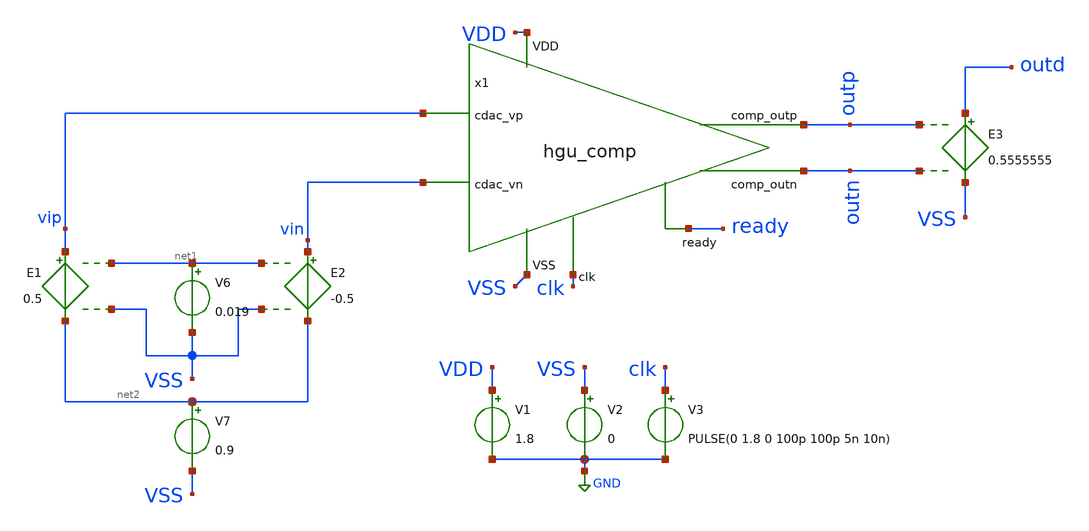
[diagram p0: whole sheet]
** sch_path: hgu/tb/tb_hgu_comp_MC_sim.sch
**.subckt tb_hgu_comp_MC_sim
x1 ready vin outp outn vip clk VDD VSS hgu_comp
V1 VDD GND 1.8
V2 VSS GND 0
V3 clk GND PULSE(0 1.8 0 100p 100p 5n 10n)
E1 vip net2 net1 VSS 0.5
E2 vin net2 net1 VSS -0.5
V6 net1 VSS 0.019
V7 net2 VSS 0.9
E3 outd VSS outp outn 0.5555555
**** begin user architecture code



.include /foss/designs/hgu_goss/hgu/spice/hgu_comp_flat_RC.spice
.lib /foss/pdks/sky130A/libs.tech/ngspice/sky130.lib.spice tt_mm
.include /foss/pdks/sky130A/libs.ref/sky130_fd_sc_hd/spice/sky130_fd_sc_hd.spice
.tran 0.1ns 10ns
.temp 25
.control
    repeat 100

    tran 0.1ns 10ns
    print avg V(outd)
    write test_mc_model.txt
    set appendwrite
    reset

    end
	meas tran v1 AVG tran1.v(outd) FROM=2n TO=10n
	meas tran v2 AVG tran2.v(outd) FROM=2n TO=10n
	meas tran v3 AVG tran3.v(outd) FROM=2n TO=10n
	meas tran v4 AVG tran4.v(outd) FROM=2n TO=10n
	meas tran v5 AVG tran5.v(outd) FROM=2n TO=10n
	meas tran v6 AVG tran6.v(outd) FROM=2n TO=10n
	meas tran v7 AVG tran7.v(outd) FROM=2n TO=10n
	meas tran v8 AVG tran8.v(outd) FROM=2n TO=10n
	meas tran v9 AVG tran9.v(outd) FROM=2n TO=10n
	meas tran v10 AVG tran10.v(outd) FROM=2n TO=10n
	let avg_v1 = (v1+v2+v3+v4+v5+v6+v7+v8+v9+v10)/10

	meas tran v11 AVG tran11.v(outd) FROM=2n TO=10n
	meas tran v12 AVG tran12.v(outd) FROM=2n TO=10n
	meas tran v13 AVG tran13.v(outd) FROM=2n TO=10n
	meas tran v14 AVG tran14.v(outd) FROM=2n TO=10n
	meas tran v15 AVG tran15.v(outd) FROM=2n TO=10n
	meas tran v16 AVG tran16.v(outd) FROM=2n TO=10n
	meas tran v17 AVG tran17.v(outd) FROM=2n TO=10n
	meas tran v18 AVG tran18.v(outd) FROM=2n TO=10n
	meas tran v19 AVG tran19.v(outd) FROM=2n TO=10n
	meas tran v20 AVG tran20.v(outd) FROM=2n TO=10n
	let avg_v2 = (v11+v12+v13+v14+v15+v16+v17+v18+v19+v20)/10


	meas tran v21 AVG tran21.v(outd) FROM=2n TO=10n
	meas tran v22 AVG tran22.v(outd) FROM=2n TO=10n
	meas tran v23 AVG tran23.v(outd) FROM=2n TO=10n
	meas tran v24 AVG tran24.v(outd) FROM=2n TO=10n
	meas tran v25 AVG tran25.v(outd) FROM=2n TO=10n
	meas tran v26 AVG tran26.v(outd) FROM=2n TO=10n
	meas tran v27 AVG tran27.v(outd) FROM=2n TO=10n
	meas tran v28 AVG tran28.v(outd) FROM=2n TO=10n
	meas tran v29 AVG tran29.v(outd) FROM=2n TO=10n
	meas tran v30 AVG tran30.v(outd) FROM=2n TO=10n
	let avg_v3 = (v21+v22+v23+v24+v25+v26+v27+v28+v29+v30)/10

	meas tran v31 AVG tran31.v(outd) FROM=2n TO=10n
	meas tran v32 AVG tran32.v(outd) FROM=2n TO=10n
	meas tran v33 AVG tran33.v(outd) FROM=2n TO=10n
	meas tran v34 AVG tran34.v(outd) FROM=2n TO=10n
	meas tran v35 AVG tran35.v(outd) FROM=2n TO=10n
	meas tran v36 AVG tran36.v(outd) FROM=2n TO=10n
	meas tran v37 AVG tran37.v(outd) FROM=2n TO=10n
	meas tran v38 AVG tran38.v(outd) FROM=2n TO=10n
	meas tran v39 AVG tran39.v(outd) FROM=2n TO=10n
	meas tran v40 AVG tran40.v(outd) FROM=2n TO=10n
	let avg_v4 = (v31+v32+v33+v34+v35+v36+v37+v38+v39+v40)/10

	meas tran v41 AVG tran41.v(outd) FROM=2n TO=10n
	meas tran v42 AVG tran42.v(outd) FROM=2n TO=10n
	meas tran v43 AVG tran43.v(outd) FROM=2n TO=10n
	meas tran v44 AVG tran44.v(outd) FROM=2n TO=10n
	meas tran v45 AVG tran45.v(outd) FROM=2n TO=10n
	meas tran v46 AVG tran46.v(outd) FROM=2n TO=10n
	meas tran v47 AVG tran47.v(outd) FROM=2n TO=10n
	meas tran v48 AVG tran48.v(outd) FROM=2n TO=10n
	meas tran v49 AVG tran49.v(outd) FROM=2n TO=10n
	meas tran v50 AVG tran50.v(outd) FROM=2n TO=10n
	let avg_v5 = (v41+v42+v43+v44+v45+v46+v47+v48+v49+v50)/10

	meas tran v51 AVG tran51.v(outd) FROM=2n TO=10n
	meas tran v52 AVG tran52.v(outd) FROM=2n TO=10n
	meas tran v53 AVG tran53.v(outd) FROM=2n TO=10n
	meas tran v54 AVG tran54.v(outd) FROM=2n TO=10n
	meas tran v55 AVG tran55.v(outd) FROM=2n TO=10n
	meas tran v56 AVG tran56.v(outd) FROM=2n TO=10n
	meas tran v57 AVG tran57.v(outd) FROM=2n TO=10n
	meas tran v58 AVG tran58.v(outd) FROM=2n TO=10n
	meas tran v59 AVG tran59.v(outd) FROM=2n TO=10n
	meas tran v60 AVG tran60.v(outd) FROM=2n TO=10n
	let avg_v6 = (v51+v52+v53+v54+v55+v56+v57+v58+v59+v60)/10

	meas tran v61 AVG tran61.v(outd) FROM=2n TO=10n
	meas tran v62 AVG tran62.v(outd) FROM=2n TO=10n
	meas tran v63 AVG tran63.v(outd) FROM=2n TO=10n
	meas tran v64 AVG tran64.v(outd) FROM=2n TO=10n
	meas tran v65 AVG tran65.v(outd) FROM=2n TO=10n
	meas tran v66 AVG tran66.v(outd) FROM=2n TO=10n
	meas tran v67 AVG tran67.v(outd) FROM=2n TO=10n
	meas tran v68 AVG tran68.v(outd) FROM=2n TO=10n
	meas tran v69 AVG tran69.v(outd) FROM=2n TO=10n
	meas tran v70 AVG tran70.v(outd) FROM=2n TO=10n
	let avg_v7 = (v61+v62+v63+v64+v65+v66+v67+v68+v69+v70)/10

	meas tran v71 AVG tran71.v(outd) FROM=2n TO=10n
	meas tran v72 AVG tran72.v(outd) FROM=2n TO=10n
	meas tran v73 AVG tran73.v(outd) FROM=2n TO=10n
	meas tran v74 AVG tran74.v(outd) FROM=2n TO=10n
	meas tran v75 AVG tran75.v(outd) FROM=2n TO=10n
	meas tran v76 AVG tran76.v(outd) FROM=2n TO=10n
	meas tran v77 AVG tran77.v(outd) FROM=2n TO=10n
	meas tran v78 AVG tran78.v(outd) FROM=2n TO=10n
	meas tran v79 AVG tran79.v(outd) FROM=2n TO=10n
	meas tran v80 AVG tran80.v(outd) FROM=2n TO=10n
	let avg_v8 = (v71+v72+v73+v74+v75+v76+v77+v78+v79+v80)/10

	meas tran v81 AVG tran81.v(outd) FROM=2n TO=10n
	meas tran v82 AVG tran82.v(outd) FROM=2n TO=10n
	meas tran v83 AVG tran83.v(outd) FROM=2n TO=10n
	meas tran v84 AVG tran84.v(outd) FROM=2n TO=10n
	meas tran v85 AVG tran85.v(outd) FROM=2n TO=10n
	meas tran v86 AVG tran86.v(outd) FROM=2n TO=10n
	meas tran v87 AVG tran87.v(outd) FROM=2n TO=10n
	meas tran v88 AVG tran88.v(outd) FROM=2n TO=10n
	meas tran v89 AVG tran89.v(outd) FROM=2n TO=10n
	meas tran v90 AVG tran90.v(outd) FROM=2n TO=10n
	let avg_v9 = (v81+v82+v83+v84+v85+v86+v87+v88+v89+v90)/10

	meas tran v91 AVG tran91.v(outd) FROM=2n TO=10n
	meas tran v92 AVG tran92.v(outd) FROM=2n TO=10n
	meas tran v93 AVG tran93.v(outd) FROM=2n TO=10n
	meas tran v94 AVG tran94.v(outd) FROM=2n TO=10n
	meas tran v95 AVG tran95.v(outd) FROM=2n TO=10n
	meas tran v96 AVG tran96.v(outd) FROM=2n TO=10n
	meas tran v97 AVG tran97.v(outd) FROM=2n TO=10n
	meas tran v98 AVG tran98.v(outd) FROM=2n TO=10n
	meas tran v99 AVG tran99.v(outd) FROM=2n TO=10n
	meas tran v100 AVG tran100.v(outd) FROM=2n TO=10n
	let avg_v10 = (v91+v92+v93+v94+v95+v96+v97+v98+v99+v100)/10

    let final_avg = (avg_v1+avg_v2+avg_v3+avg_v4+avg_v5+avg_v6+avg_v7+avg_v8+avg_v9+avg_v10)/10
    *plot all.v(outd)
    print final_avg
.endc
.save all


**** end user architecture code
**.ends

* expanding   symbol:  ../xschem/hgu_comp.sym # of pins=8
** sym_path: hgu/xschem/hgu_comp.sym
** sch_path: hgu/xschem/hgu_comp.sch
.subckt hgu_comp ready cdac_vn comp_outp comp_outn cdac_vp clk VDD VSS
*.ipin cdac_vn
*.ipin cdac_vp
*.ipin VSS
*.ipin VDD
*.ipin clk
*.opin ready
*.opin comp_outp
*.opin comp_outn
XM1 net1 clk VSS VSS sky130_fd_pr__nfet_01v8 L=0.15 W=4 nf=4 ad='int((nf+1)/2) * W/nf * 0.29' as='int((nf+2)/2) * W/nf * 0.29'
+ pd='2*int((nf+1)/2) * (W/nf + 0.29)' ps='2*int((nf+2)/2) * (W/nf + 0.29)' nrd='0.29 / W' nrs='0.29 / W'
+ sa=0 sb=0 sd=0 mult=1 m=1
XM4 Y X Q VSS sky130_fd_pr__nfet_01v8 L=0.15 W=1 nf=1 ad='int((nf+1)/2) * W/nf * 0.29' as='int((nf+2)/2) * W/nf * 0.29'
+ pd='2*int((nf+1)/2) * (W/nf + 0.29)' ps='2*int((nf+2)/2) * (W/nf + 0.29)' nrd='0.29 / W' nrs='0.29 / W'
+ sa=0 sb=0 sd=0 mult=1 m=1
XM5 X Y P VSS sky130_fd_pr__nfet_01v8 L=0.15 W=1 nf=1 ad='int((nf+1)/2) * W/nf * 0.29' as='int((nf+2)/2) * W/nf * 0.29'
+ pd='2*int((nf+1)/2) * (W/nf + 0.29)' ps='2*int((nf+2)/2) * (W/nf + 0.29)' nrd='0.29 / W' nrs='0.29 / W'
+ sa=0 sb=0 sd=0 mult=1 m=1
XM6 X Y VDD VDD sky130_fd_pr__pfet_01v8 L=0.15 W=1 nf=1 ad='int((nf+1)/2) * W/nf * 0.29' as='int((nf+2)/2) * W/nf * 0.29'
+ pd='2*int((nf+1)/2) * (W/nf + 0.29)' ps='2*int((nf+2)/2) * (W/nf + 0.29)' nrd='0.29 / W' nrs='0.29 / W'
+ sa=0 sb=0 sd=0 mult=1 m=1
XM7 Y X VDD VDD sky130_fd_pr__pfet_01v8 L=0.15 W=1 nf=1 ad='int((nf+1)/2) * W/nf * 0.29' as='int((nf+2)/2) * W/nf * 0.29'
+ pd='2*int((nf+1)/2) * (W/nf + 0.29)' ps='2*int((nf+2)/2) * (W/nf + 0.29)' nrd='0.29 / W' nrs='0.29 / W'
+ sa=0 sb=0 sd=0 mult=1 m=1
XM8 X clk VDD VDD sky130_fd_pr__pfet_01v8 L=0.15 W=1 nf=1 ad='int((nf+1)/2) * W/nf * 0.29' as='int((nf+2)/2) * W/nf * 0.29'
+ pd='2*int((nf+1)/2) * (W/nf + 0.29)' ps='2*int((nf+2)/2) * (W/nf + 0.29)' nrd='0.29 / W' nrs='0.29 / W'
+ sa=0 sb=0 sd=0 mult=1 m=1
XM9 P clk VDD VDD sky130_fd_pr__pfet_01v8 L=0.15 W=1 nf=1 ad='int((nf+1)/2) * W/nf * 0.29' as='int((nf+2)/2) * W/nf * 0.29'
+ pd='2*int((nf+1)/2) * (W/nf + 0.29)' ps='2*int((nf+2)/2) * (W/nf + 0.29)' nrd='0.29 / W' nrs='0.29 / W'
+ sa=0 sb=0 sd=0 mult=1 m=1
XM10 Y clk VDD VDD sky130_fd_pr__pfet_01v8 L=0.15 W=1 nf=1 ad='int((nf+1)/2) * W/nf * 0.29' as='int((nf+2)/2) * W/nf * 0.29'
+ pd='2*int((nf+1)/2) * (W/nf + 0.29)' ps='2*int((nf+2)/2) * (W/nf + 0.29)' nrd='0.29 / W' nrs='0.29 / W'
+ sa=0 sb=0 sd=0 mult=1 m=1
XM11 Q clk VDD VDD sky130_fd_pr__pfet_01v8 L=0.15 W=1 nf=1 ad='int((nf+1)/2) * W/nf * 0.29' as='int((nf+2)/2) * W/nf * 0.29'
+ pd='2*int((nf+1)/2) * (W/nf + 0.29)' ps='2*int((nf+2)/2) * (W/nf + 0.29)' nrd='0.29 / W' nrs='0.29 / W'
+ sa=0 sb=0 sd=0 mult=1 m=1
XM16 RS_n RS_p VDD VDD sky130_fd_pr__pfet_01v8 L=0.15 W=0.84 nf=1 ad='int((nf+1)/2) * W/nf * 0.29' as='int((nf+2)/2) * W/nf * 0.29'
+ pd='2*int((nf+1)/2) * (W/nf + 0.29)' ps='2*int((nf+2)/2) * (W/nf + 0.29)' nrd='0.29 / W' nrs='0.29 / W'
+ sa=0 sb=0 sd=0 mult=1 m=1
XM17 RS_p RS_n VDD VDD sky130_fd_pr__pfet_01v8 L=0.15 W=0.84 nf=1 ad='int((nf+1)/2) * W/nf * 0.29' as='int((nf+2)/2) * W/nf * 0.29'
+ pd='2*int((nf+1)/2) * (W/nf + 0.29)' ps='2*int((nf+2)/2) * (W/nf + 0.29)' nrd='0.29 / W' nrs='0.29 / W'
+ sa=0 sb=0 sd=0 mult=1 m=1
XM19 RS_p Y_inv VSS VSS sky130_fd_pr__nfet_01v8 L=0.15 W=0.84 nf=1 ad='int((nf+1)/2) * W/nf * 0.29' as='int((nf+2)/2) * W/nf * 0.29'
+ pd='2*int((nf+1)/2) * (W/nf + 0.29)' ps='2*int((nf+2)/2) * (W/nf + 0.29)' nrd='0.29 / W' nrs='0.29 / W'
+ sa=0 sb=0 sd=0 mult=1 m=1
XM23 RS_n X_inv VSS VSS sky130_fd_pr__nfet_01v8 L=0.15 W=0.84 nf=1 ad='int((nf+1)/2) * W/nf * 0.29' as='int((nf+2)/2) * W/nf * 0.29'
+ pd='2*int((nf+1)/2) * (W/nf + 0.29)' ps='2*int((nf+2)/2) * (W/nf + 0.29)' nrd='0.29 / W' nrs='0.29 / W'
+ sa=0 sb=0 sd=0 mult=1 m=1
XM2 P cdac_vp net1 VSS sky130_fd_pr__nfet_01v8_lvt L=0.15 W=8 nf=8 ad='int((nf+1)/2) * W / nf * 0.29'
+ as='int((nf+2)/2) * W / nf * 0.29' pd='2*int((nf+1)/2) * (W / nf + 0.29)' ps='2*int((nf+2)/2) * (W / nf + 0.29)'
+ nrd='0.29 / W ' nrs='0.29 / W ' sa=0 sb=0 sd=0 mult=1 m=1
XM3 Q cdac_vn net1 VSS sky130_fd_pr__nfet_01v8_lvt L=0.15 W=8 nf=8 ad='int((nf+1)/2) * W / nf * 0.29'
+ as='int((nf+2)/2) * W / nf * 0.29' pd='2*int((nf+1)/2) * (W / nf + 0.29)' ps='2*int((nf+2)/2) * (W / nf + 0.29)'
+ nrd='0.29 / W ' nrs='0.29 / W ' sa=0 sb=0 sd=0 mult=1 m=1
XM12 X_inv X VDD VDD sky130_fd_pr__pfet_01v8 L=0.15 W=0.84 nf=1 ad='int((nf+1)/2) * W/nf * 0.29' as='int((nf+2)/2) * W/nf * 0.29'
+ pd='2*int((nf+1)/2) * (W/nf + 0.29)' ps='2*int((nf+2)/2) * (W/nf + 0.29)' nrd='0.29 / W' nrs='0.29 / W'
+ sa=0 sb=0 sd=0 mult=1 m=1
XM13 X_inv X VSS VSS sky130_fd_pr__nfet_01v8 L=0.15 W=0.42 nf=1 ad='int((nf+1)/2) * W/nf * 0.29' as='int((nf+2)/2) * W/nf * 0.29'
+ pd='2*int((nf+1)/2) * (W/nf + 0.29)' ps='2*int((nf+2)/2) * (W/nf + 0.29)' nrd='0.29 / W' nrs='0.29 / W'
+ sa=0 sb=0 sd=0 mult=1 m=1
XM14 X_drive X_inv VDD VDD sky130_fd_pr__pfet_01v8 L=0.15 W=2.52 nf=3 ad='int((nf+1)/2) * W/nf * 0.29'
+ as='int((nf+2)/2) * W/nf * 0.29' pd='2*int((nf+1)/2) * (W/nf + 0.29)' ps='2*int((nf+2)/2) * (W/nf + 0.29)'
+ nrd='0.29 / W' nrs='0.29 / W' sa=0 sb=0 sd=0 mult=1 m=1
XM15 X_drive X_inv VSS VSS sky130_fd_pr__nfet_01v8 L=0.15 W=1.38 nf=3 ad='int((nf+1)/2) * W/nf * 0.29'
+ as='int((nf+2)/2) * W/nf * 0.29' pd='2*int((nf+1)/2) * (W/nf + 0.29)' ps='2*int((nf+2)/2) * (W/nf + 0.29)'
+ nrd='0.29 / W' nrs='0.29 / W' sa=0 sb=0 sd=0 mult=1 m=1
XM18 Y_inv Y VDD VDD sky130_fd_pr__pfet_01v8 L=0.15 W=0.84 nf=1 ad='int((nf+1)/2) * W/nf * 0.29' as='int((nf+2)/2) * W/nf * 0.29'
+ pd='2*int((nf+1)/2) * (W/nf + 0.29)' ps='2*int((nf+2)/2) * (W/nf + 0.29)' nrd='0.29 / W' nrs='0.29 / W'
+ sa=0 sb=0 sd=0 mult=1 m=1
XM20 Y_inv Y VSS VSS sky130_fd_pr__nfet_01v8 L=0.15 W=0.42 nf=1 ad='int((nf+1)/2) * W/nf * 0.29' as='int((nf+2)/2) * W/nf * 0.29'
+ pd='2*int((nf+1)/2) * (W/nf + 0.29)' ps='2*int((nf+2)/2) * (W/nf + 0.29)' nrd='0.29 / W' nrs='0.29 / W'
+ sa=0 sb=0 sd=0 mult=1 m=1
XM21 Y_drive Y_inv VDD VDD sky130_fd_pr__pfet_01v8 L=0.15 W=2.52 nf=3 ad='int((nf+1)/2) * W/nf * 0.29'
+ as='int((nf+2)/2) * W/nf * 0.29' pd='2*int((nf+1)/2) * (W/nf + 0.29)' ps='2*int((nf+2)/2) * (W/nf + 0.29)'
+ nrd='0.29 / W' nrs='0.29 / W' sa=0 sb=0 sd=0 mult=1 m=1
XM22 Y_drive Y_inv VSS VSS sky130_fd_pr__nfet_01v8 L=0.15 W=1.38 nf=3 ad='int((nf+1)/2) * W/nf * 0.29'
+ as='int((nf+2)/2) * W/nf * 0.29' pd='2*int((nf+1)/2) * (W/nf + 0.29)' ps='2*int((nf+2)/2) * (W/nf + 0.29)'
+ nrd='0.29 / W' nrs='0.29 / W' sa=0 sb=0 sd=0 mult=1 m=1
XM24 net2 Y_drive X_drive VDD sky130_fd_pr__pfet_01v8 L=0.15 W=0.84 nf=1 ad='int((nf+1)/2) * W/nf * 0.29'
+ as='int((nf+2)/2) * W/nf * 0.29' pd='2*int((nf+1)/2) * (W/nf + 0.29)' ps='2*int((nf+2)/2) * (W/nf + 0.29)'
+ nrd='0.29 / W' nrs='0.29 / W' sa=0 sb=0 sd=0 mult=1 m=1
XM25 net2 X_drive Y_drive VDD sky130_fd_pr__pfet_01v8 L=0.15 W=0.84 nf=1 ad='int((nf+1)/2) * W/nf * 0.29'
+ as='int((nf+2)/2) * W/nf * 0.29' pd='2*int((nf+1)/2) * (W/nf + 0.29)' ps='2*int((nf+2)/2) * (W/nf + 0.29)'
+ nrd='0.29 / W' nrs='0.29 / W' sa=0 sb=0 sd=0 mult=1 m=1
XM26 net2 Y_drive net3 VSS sky130_fd_pr__nfet_01v8 L=0.15 W=0.84 nf=1 ad='int((nf+1)/2) * W/nf * 0.29'
+ as='int((nf+2)/2) * W/nf * 0.29' pd='2*int((nf+1)/2) * (W/nf + 0.29)' ps='2*int((nf+2)/2) * (W/nf + 0.29)'
+ nrd='0.29 / W' nrs='0.29 / W' sa=0 sb=0 sd=0 mult=1 m=1
XM27 net3 X_drive VSS VSS sky130_fd_pr__nfet_01v8 L=0.15 W=0.84 nf=1 ad='int((nf+1)/2) * W/nf * 0.29'
+ as='int((nf+2)/2) * W/nf * 0.29' pd='2*int((nf+1)/2) * (W/nf + 0.29)' ps='2*int((nf+2)/2) * (W/nf + 0.29)'
+ nrd='0.29 / W' nrs='0.29 / W' sa=0 sb=0 sd=0 mult=1 m=1
XM28 ready net2 VDD VDD sky130_fd_pr__pfet_01v8 L=0.15 W=0.84 nf=1 ad='int((nf+1)/2) * W/nf * 0.29' as='int((nf+2)/2) * W/nf * 0.29'
+ pd='2*int((nf+1)/2) * (W/nf + 0.29)' ps='2*int((nf+2)/2) * (W/nf + 0.29)' nrd='0.29 / W' nrs='0.29 / W'
+ sa=0 sb=0 sd=0 mult=1 m=1
XM29 ready net2 VSS VSS sky130_fd_pr__nfet_01v8 L=0.15 W=0.42 nf=1 ad='int((nf+1)/2) * W/nf * 0.29' as='int((nf+2)/2) * W/nf * 0.29'
+ pd='2*int((nf+1)/2) * (W/nf + 0.29)' ps='2*int((nf+2)/2) * (W/nf + 0.29)' nrd='0.29 / W' nrs='0.29 / W'
+ sa=0 sb=0 sd=0 mult=1 m=1
XM30 net4 RS_p VDD VDD sky130_fd_pr__pfet_01v8 L=0.15 W=0.84 nf=1 ad='int((nf+1)/2) * W/nf * 0.29' as='int((nf+2)/2) * W/nf * 0.29'
+ pd='2*int((nf+1)/2) * (W/nf + 0.29)' ps='2*int((nf+2)/2) * (W/nf + 0.29)' nrd='0.29 / W' nrs='0.29 / W'
+ sa=0 sb=0 sd=0 mult=1 m=1
XM31 net4 RS_p VSS VSS sky130_fd_pr__nfet_01v8 L=0.15 W=0.42 nf=1 ad='int((nf+1)/2) * W/nf * 0.29' as='int((nf+2)/2) * W/nf * 0.29'
+ pd='2*int((nf+1)/2) * (W/nf + 0.29)' ps='2*int((nf+2)/2) * (W/nf + 0.29)' nrd='0.29 / W' nrs='0.29 / W'
+ sa=0 sb=0 sd=0 mult=1 m=1
XM32 comp_outp net4 VDD VDD sky130_fd_pr__pfet_01v8 L=0.15 W=2.52 nf=3 ad='int((nf+1)/2) * W/nf * 0.29'
+ as='int((nf+2)/2) * W/nf * 0.29' pd='2*int((nf+1)/2) * (W/nf + 0.29)' ps='2*int((nf+2)/2) * (W/nf + 0.29)'
+ nrd='0.29 / W' nrs='0.29 / W' sa=0 sb=0 sd=0 mult=1 m=1
XM33 comp_outp net4 VSS VSS sky130_fd_pr__nfet_01v8 L=0.15 W=1.38 nf=3 ad='int((nf+1)/2) * W/nf * 0.29'
+ as='int((nf+2)/2) * W/nf * 0.29' pd='2*int((nf+1)/2) * (W/nf + 0.29)' ps='2*int((nf+2)/2) * (W/nf + 0.29)'
+ nrd='0.29 / W' nrs='0.29 / W' sa=0 sb=0 sd=0 mult=1 m=1
XM34 net5 RS_n VDD VDD sky130_fd_pr__pfet_01v8 L=0.15 W=0.84 nf=1 ad='int((nf+1)/2) * W/nf * 0.29' as='int((nf+2)/2) * W/nf * 0.29'
+ pd='2*int((nf+1)/2) * (W/nf + 0.29)' ps='2*int((nf+2)/2) * (W/nf + 0.29)' nrd='0.29 / W' nrs='0.29 / W'
+ sa=0 sb=0 sd=0 mult=1 m=1
XM35 net5 RS_n VSS VSS sky130_fd_pr__nfet_01v8 L=0.15 W=0.42 nf=1 ad='int((nf+1)/2) * W/nf * 0.29' as='int((nf+2)/2) * W/nf * 0.29'
+ pd='2*int((nf+1)/2) * (W/nf + 0.29)' ps='2*int((nf+2)/2) * (W/nf + 0.29)' nrd='0.29 / W' nrs='0.29 / W'
+ sa=0 sb=0 sd=0 mult=1 m=1
XM36 comp_outn net5 VDD VDD sky130_fd_pr__pfet_01v8 L=0.15 W=2.52 nf=3 ad='int((nf+1)/2) * W/nf * 0.29'
+ as='int((nf+2)/2) * W/nf * 0.29' pd='2*int((nf+1)/2) * (W/nf + 0.29)' ps='2*int((nf+2)/2) * (W/nf + 0.29)'
+ nrd='0.29 / W' nrs='0.29 / W' sa=0 sb=0 sd=0 mult=1 m=1
XM37 comp_outn net5 VSS VSS sky130_fd_pr__nfet_01v8 L=0.15 W=1.38 nf=3 ad='int((nf+1)/2) * W/nf * 0.29'
+ as='int((nf+2)/2) * W/nf * 0.29' pd='2*int((nf+1)/2) * (W/nf + 0.29)' ps='2*int((nf+2)/2) * (W/nf + 0.29)'
+ nrd='0.29 / W' nrs='0.29 / W' sa=0 sb=0 sd=0 mult=1 m=1
.ends

.GLOBAL GND
.end
